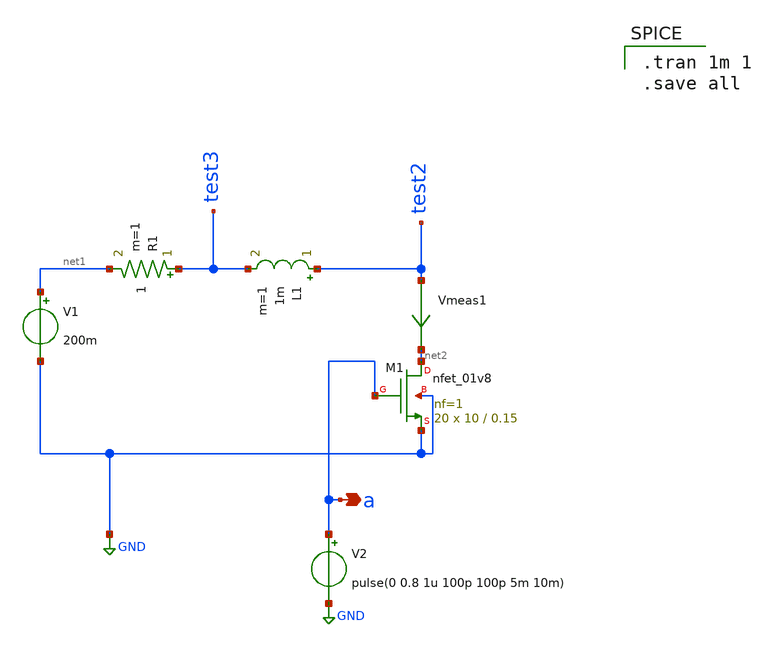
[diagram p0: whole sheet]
** sch_path: component/Core Functionality of boost Converter/vs test3.sch
**.subckt vs test3 a
*.opin a
V1 net1 GND 200m
L1 test2 test3 1m m=1
XM1 net2 a GND GND sky130_fd_pr__nfet_01v8 L=0.15 W=10 nf=1 ad='int((nf+1)/2) * W/nf * 0.29' as='int((nf+2)/2) * W/nf * 0.29'
+ pd='2*int((nf+1)/2) * (W/nf + 0.29)' ps='2*int((nf+2)/2) * (W/nf + 0.29)' nrd='0.29 / W' nrs='0.29 / W'
+ sa=0 sb=0 sd=0 mult=20 m=20
V2 a GND pulse(0 0.8 1u 100p 100p 5m 10m)
R1 test3 net1 1 m=1
Vmeas1 test2 net2 0
.save i(vmeas1)
**** begin user architecture code

** opencircuitdesign pdks install
.lib $::SKYWATER_MODELS/sky130.lib.spice tt



.tran 1m 1
.save all

**** end user architecture code
**.ends
.GLOBAL GND
.end
